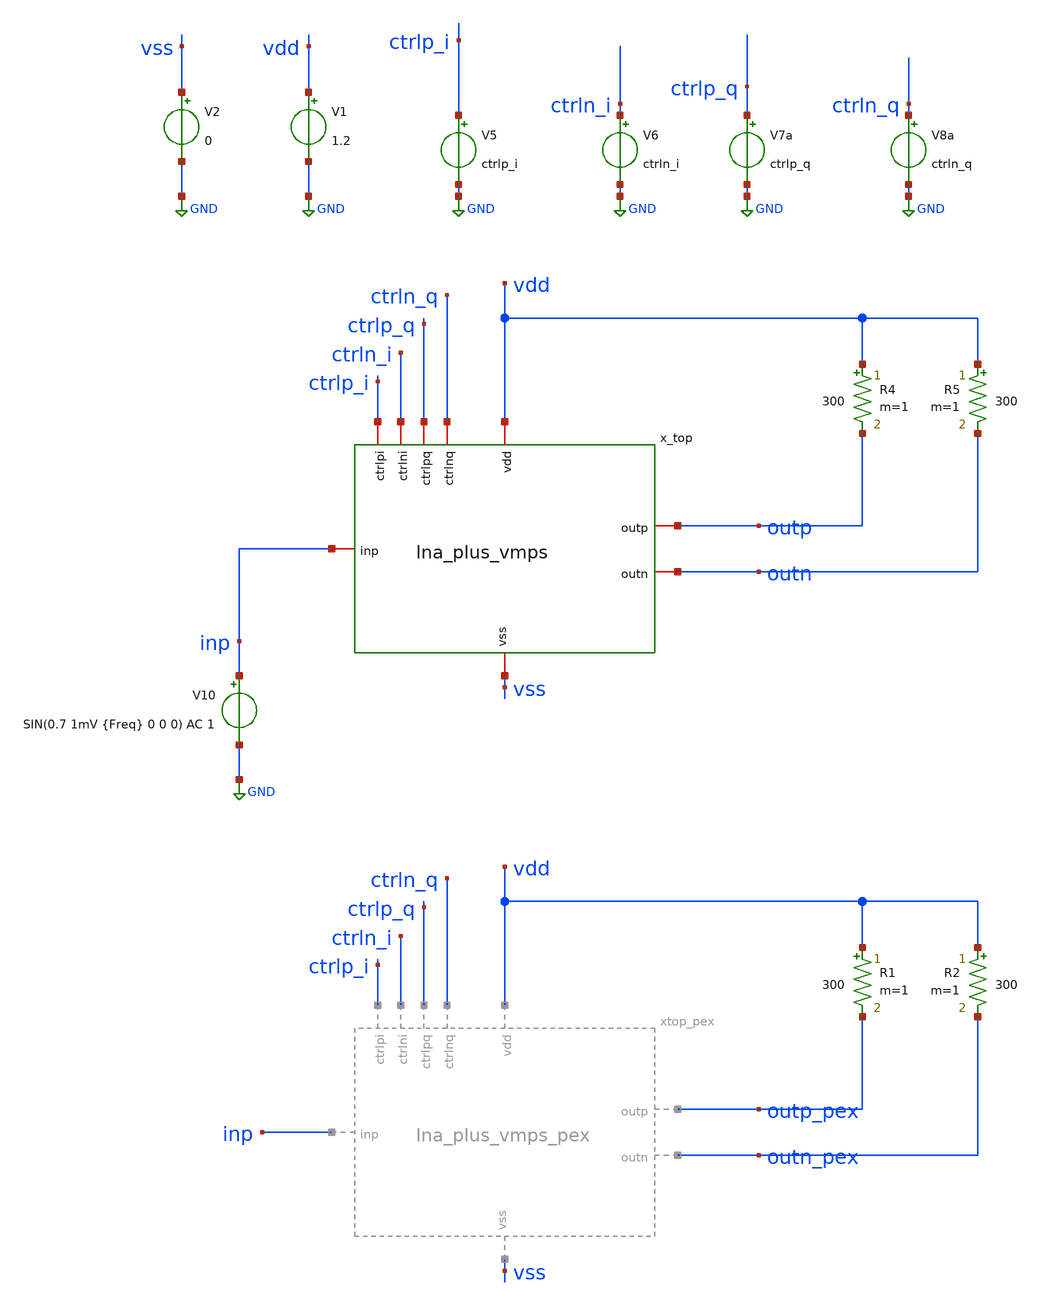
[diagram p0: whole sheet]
** sch_path: LNA7096-main/schematic/xschem/06_integ/lna_plus_vmps_tb.sch
**.subckt lna_plus_vmps_tb
V1 vdd GND 1.2
V5 ctrlp_i GND ctrlp_i
V6 ctrln_i GND ctrln_i
V7a ctrlp_q GND ctrlp_q
V8a ctrln_q GND ctrln_q
V10 inp GND SIN(0.7 1mV {Freq} 0 0 0) AC 1
R4 vdd outp 300 m=1
R5 vdd outn 300 m=1
x_top vdd ctrlp_i ctrlp_q ctrln_q ctrln_i outp inp outn vss lna_plus_vmps
V2 vss GND 0
R1 vdd outp_pex 300 m=1
R2 vdd outn_pex 300 m=1
**** begin user architecture code

.lib cornerCAP.lib cap_typ
.lib cornerMOSlv.lib mos_tt
.lib cornerMOShv.lib mos_tt
.lib cornerHBT.lib hbt_typ
.lib cornerRES.lib res_typ
.lib cornerDIO.lib dio_tt

.include /home/ic_design_trg/pdk/ihp-sg13g2/libs.ref/sg13g2_stdcell/spice/sg13g2_stdcell.spice



.include /home/ic_design_trg/lna_ihp/xschem/06_integ/simulation/lna_vmps.save
.temp=27


.param ctrlp_i=0.6 ctrln_i=0.9
.param ctrlp_q=0.6 ctrln_q=0.6

.param VDD_val = 1.2
.param CM_rf = 0.6
.param freq = 1.17645G

.control
*  --- 0. Setup and Initialization ---
*  Save the required nodes including the input node 'inp' to conserve memory
*  [UPDATED] Added the PEX output nodes to the save list
save v(outp) v(outn) v(inp) v(x_top.lna_out) v(x_top.x_vmps.x_vga_i.inp_a)
+ v(x_top.x_vmps.x_vga_i.inn_a) v(outp_pex) v(outn_pex)

*  Unset appendwrite initially to ensure we create a fresh file
unset appendwrite

*  --- 1. Define Phase Angle and Control Vectors ---
compose theta_vals start=0 stop=360 step=5.625
let rad_vec = theta_vals * pi / 180

*  Define Constants
let v_cm = 0.6
let v_max = 0.3
let gamma = 1.30

*  --- 2. PRE-DISTORTION SETTING ---
let cos_w = cos(rad_vec)
let sin_w = sin(rad_vec)

*  Use 'gt' and 'lt' to emulate sgn()
let sgn_cos = (cos_w gt 0) - (cos_w lt 0)
let sgn_sin = (sin_w gt 0) - (sin_w lt 0)

*  Apply Power-Law Mapping
let i_corr = sgn_cos * (abs(cos_w)^gamma)
let q_corr = sgn_sin * (abs(sin_w)^gamma)

*  Pre-calculate 4-Quadrant Control Voltages
let pi_p_vec = v_cm + v_max * i_corr
let pi_n_vec = v_cm - v_max * i_corr
let pq_p_vec = v_cm + v_max * q_corr
let pq_n_vec = v_cm - v_max * q_corr

*  --- 3. Initialize Loop ---
let n_runs = length(theta_vals)
let run_idx = 0

*  Capture the start plot (constants) to retrieve vectors later
set start_plot = $curplot

*  Create CSV File Headers for both Schematic and PEX data
echo theta, ctrlp_i, ctrln_i, ctrlp_q, ctrln_q, mag_diff_db, phase_diff_deg, gain_db >
+ vmps_sweep.csv
echo theta, ctrlp_i, ctrln_i, ctrlp_q, ctrln_q, mag_diff_db_pex, phase_diff_deg_pex, gain_db_pex >
+ vmps_sweep_pex.csv

*  --- 4. Execution Loop ---
dowhile run_idx < n_runs
    *  A. Retrieve calculated DC voltages from the start plot
    let pip_act = {$start_plot}.pi_p_vec[run_idx]
    let pin_act = {$start_plot}.pi_n_vec[run_idx]
    let pqp_act = {$start_plot}.pq_p_vec[run_idx]
    let pqn_act = {$start_plot}.pq_n_vec[run_idx]
    let t_act = {$start_plot}.theta_vals[run_idx]

    *  B. Apply Bias
    alter V5 dc = $&pip_act
    alter V6 dc = $&pin_act
    alter V7a dc = $&pqp_act
    alter V8a dc = $&pqn_act

    *  C. Operating Point Analysis (OP)
    op
    remzerovec

    *  Save OP results to RAW file
    if run_idx = 0
        write lna_vmps.raw all
        set appendwrite
    else
        write lna_vmps.raw all
    end
    destroy $curplot

    *  D. AC Simulation
    ac lin 200 0.1G 2.5G

        * ==========================================
        * 1. Schematic (x_top) Calculations
        * ==========================================
        let vdiff_out = v(outp) - v(outn)
        let mag_diff = db(vdiff_out)
        let ph_diff = cph(vdiff_out) * 180 / pi
        let gain_linear = vdiff_out / v(inp)
        let gain_db_vec = db(gain_linear)

        * Measure at Fundamental Frequency (1.17645 GHz)
        meas ac mag_diff_db find mag_diff at=1.17645e9
        meas ac phase_diff_deg find ph_diff at=1.17645e9
        meas ac gain_db find gain_db_vec at=1.17645e9

        * Prepare vectors for saving
        let vdiff_db = db(vdiff_out)
        let vdiff_phase_unwrap = cph(vdiff_out) * 180 / pi

        * ==========================================
        * 2. Extracted (xtop_pex) Calculations
        * ==========================================
        let vdiff_out_pex = v(outp_pex) - v(outn_pex)
        let mag_diff_pex = db(vdiff_out_pex)
        let ph_diff_pex = cph(vdiff_out_pex) * 180 / pi
        let gain_linear_pex = vdiff_out_pex / v(inp)
        let gain_db_vec_pex = db(gain_linear_pex)

        * Measure at Fundamental Frequency (1.17645 GHz)
        meas ac mag_diff_db_pex find mag_diff_pex at=1.17645e9
        meas ac phase_diff_deg_pex find ph_diff_pex at=1.17645e9
        meas ac gain_db_pex find gain_db_vec_pex at=1.17645e9

        * Prepare vectors for saving
        let vdiff_db_pex = db(vdiff_out_pex)
        let vdiff_phase_unwrap_pex = cph(vdiff_out_pex) * 180 / pi

        * ==========================================
        * 3. Write Results
        * ==========================================
        * Write Control Voltages and Measured values to the respective CSVs
        echo $&t_act, $&pip_act, $&pin_act, $&pqp_act, $&pqn_act, $&mag_diff_db, $&phase_diff_deg,
+ $&gain_db >> vmps_sweep.csv
        echo $&t_act, $&pip_act, $&pin_act, $&pqp_act, $&pqn_act, $&mag_diff_db_pex,
+ $&phase_diff_deg_pex, $&gain_db_pex >> vmps_sweep_pex.csv

        * Save AC results to RAW file (appending sequentially)
        * [UPDATED] Included PEX differential vectors and nodes into the raw file write
        write lna_vmps.raw v(outp) v(outn) v(inp) vdiff_out vdiff_db vdiff_phase_unwrap gain_db_vec
+ v(x_top.lna_out) v(x_top.x_vmps.x_vga_i.inp_a) v(x_top.x_vmps.x_vga_i.inn_a) v(outp_pex) v(outn_pex) vdiff_out_pex
+ vdiff_db_pex vdiff_phase_unwrap_pex gain_db_vec_pex

        destroy $curplot

        *  E. Transient Simulation (NEW)
***    tran 0.01n 20n

    let run_idx = run_idx + 1
end
.endc


**** end user architecture code
**.ends
.GLOBAL GND
.end
